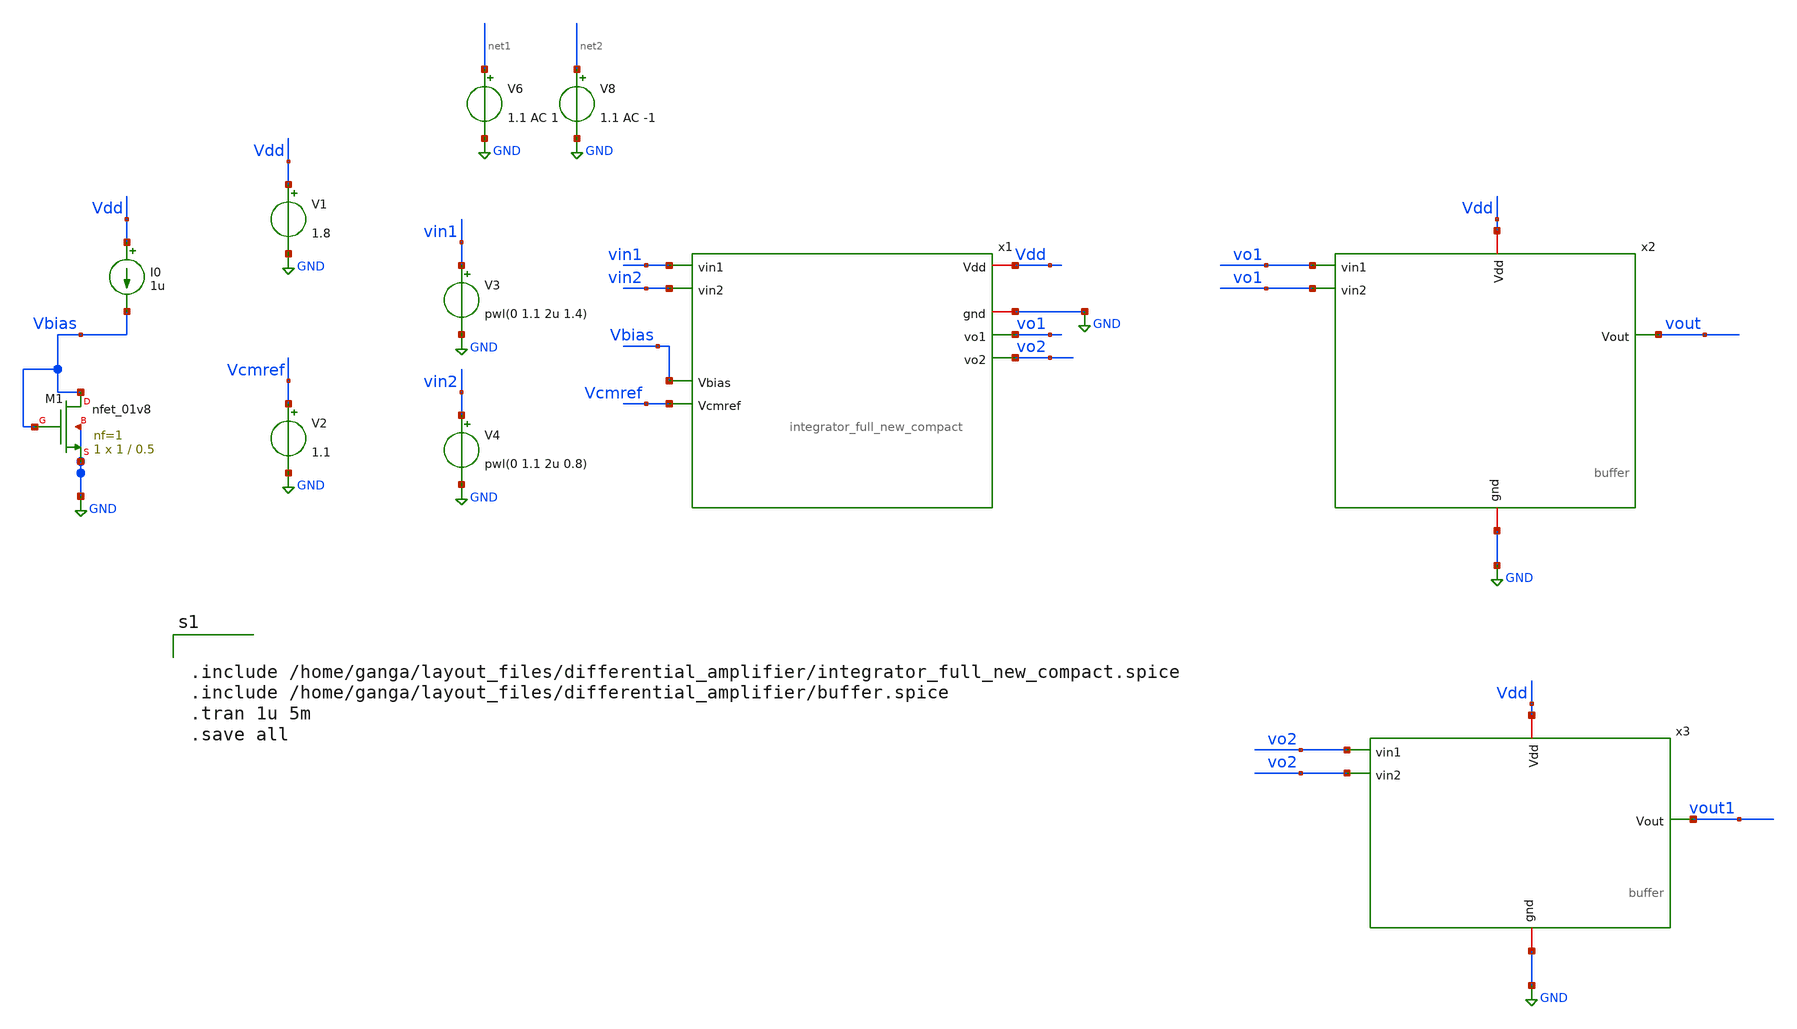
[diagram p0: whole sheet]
** sch_path: xschem/xschemfiles/integratortest.sch
**.subckt integratortest
V3 vin1 GND pwl(0 1.1 2u 1.4)
V4 vin2 GND pwl(0 1.1 2u 0.8)
V2 Vcmref GND 1.1
I0 Vdd Vbias 1u
V1 Vdd GND 1.8
x2 vo1 vo1 GND Vdd vout buffer
x3 vo2 vo2 GND Vdd vout1 buffer
XM1 Vbias Vbias GND GND sky130_fd_pr__nfet_01v8 L=0.5 W=1 nf=1 ad='int((nf+1)/2) * W/nf * 0.29' as='int((nf+2)/2) * W/nf * 0.29'
+ pd='2*int((nf+1)/2) * (W/nf + 0.29)' ps='2*int((nf+2)/2) * (W/nf + 0.29)' nrd='0.29 / W' nrs='0.29 / W'
+ sa=0 sb=0 sd=0 mult=1 m=1
V6 net1 GND 1.1 AC 1
V8 net2 GND 1.1 AC -1
x1 Vdd GND vin1 vin2 Vbias Vcmref vo2 vo1 integrator_full_new_compact
**** begin user architecture code


.include /home/ganga/layout_files/differential_amplifier/integrator_full_new_compact.spice
.include /home/ganga/layout_files/differential_amplifier/buffer.spice
.tran 1u 5m
.save all



** opencircuitdesign pdks install
.lib $::SKYWATER_MODELS/sky130.lib.spice tt


**** end user architecture code
**.ends
.GLOBAL GND
.end
